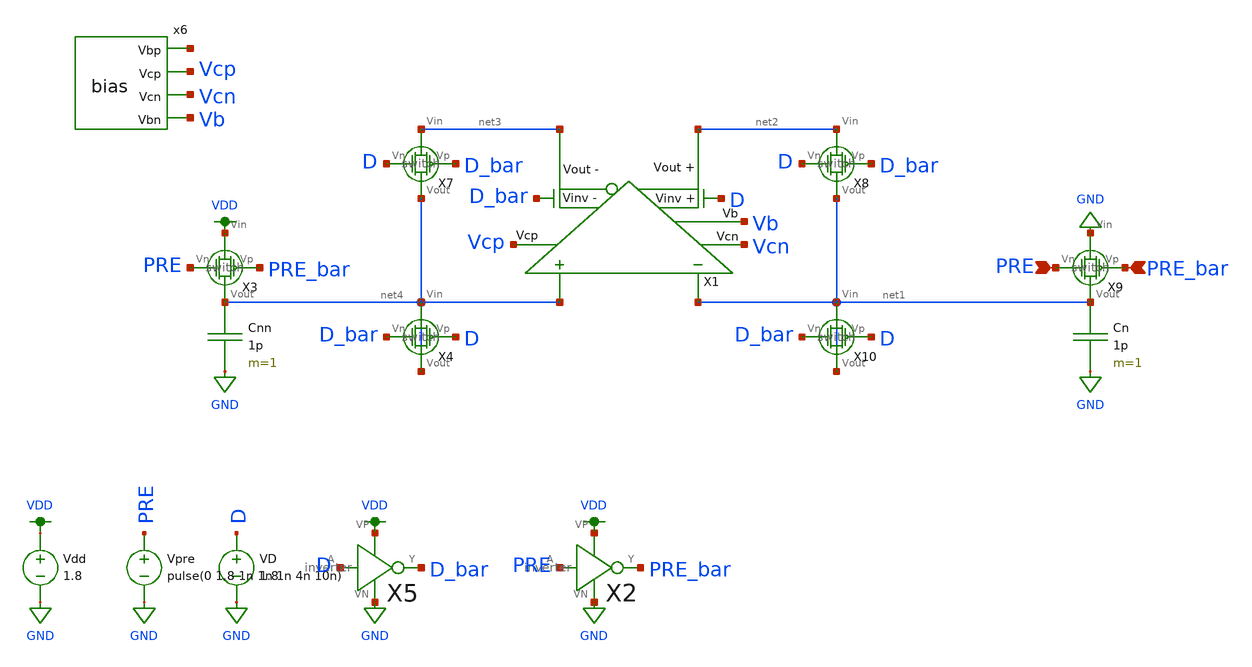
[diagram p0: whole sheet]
** sch_path: simulations/helpppp.sch
**.subckt helpppp PRE_bar PRE
*.ipin PRE_bar
*.ipin PRE
X1 D_bar net3 net2 Vcp Vb net1 net4 D Vcn ota W_U=12 L_U=0.5
Cn net1 GND 1p m=1
Cnn net4 GND 1p m=1
Vdd VDD GND 1.8
Vpre PRE GND pulse(0 1.8 1n 1n 1n 4n 10n)
X2 PRE PRE_bar VDD GND inverter
X5 D D_bar VDD GND inverter
VD D GND 1.8
x6 net5 Vcp Vcn Vb bias
X3 VDD net4 PRE_bar PRE switch W_U=12 L_U=0.5
X4 net4 net4 D D_bar switch W_U=12 L_U=0.5
X7 net3 net4 D_bar D switch W_U=12 L_U=0.5
X8 net2 net1 D_bar D switch W_U=12 L_U=0.5
X9 GND net1 PRE_bar PRE switch W_U=12 L_U=0.5
X10 net1 net1 D D_bar switch W_U=12 L_U=0.5
**** begin user architecture code

.option wnflag=1
.param MC_SWITCH=0.0
.lib ~/skywater/skywater-pdk/libraries/sky130_fd_pr_ngspice/latest/models/sky130.lib.spice tt


.tran 0.01n 200n
.save all

**** end user architecture code
**.ends

* expanding   symbol:  ../schematics/ota.sym # of pins=9
** sym_path: schematics/ota.sym
** sch_path: schematics/ota.sch
.subckt ota Vinv_n Vout_n Vout_p Vcp Vb Vin_n Vin_p Vinv_p Vcn  L_U=0.15 W_U=1
*.ipin Vin_n
*.ipin Vin_p
*.opin Vout_n
*.opin Vout_p
*.ipin Vcp
*.ipin Vb
*.ipin Vinv_p
*.ipin Vinv_n
*.ipin Vcn
XM18 net3 net3 VDD VDD sky130_fd_pr__pfet_01v8 L=L_U W=W_U nf=1 ad='int((nf+1)/2) * W/nf * 0.29' as='int((nf+2)/2) * W/nf * 0.29'
+ pd='2*int((nf+1)/2) * (W/nf + 0.29)' ps='2*int((nf+2)/2) * (W/nf + 0.29)' nrd='0.29 / W' nrs='0.29 / W'
+ sa=0 sb=0 sd=0 mult=1 m=1
XM19 net4 Vin_n net1 GND sky130_fd_pr__nfet_01v8 L=L_U W=W_U nf=1 ad='int((nf+1)/2) * W/nf * 0.29' as='int((nf+2)/2) * W/nf * 0.29'
+ pd='2*int((nf+1)/2) * (W/nf + 0.29)' ps='2*int((nf+2)/2) * (W/nf + 0.29)' nrd='0.29 / W' nrs='0.29 / W'
+ sa=0 sb=0 sd=0 mult=1 m=1
XM20 net3 Vin_p net1 GND sky130_fd_pr__nfet_01v8 L=L_U W=W_U nf=1 ad='int((nf+1)/2) * W/nf * 0.29' as='int((nf+2)/2) * W/nf * 0.29'
+ pd='2*int((nf+1)/2) * (W/nf + 0.29)' ps='2*int((nf+2)/2) * (W/nf + 0.29)' nrd='0.29 / W' nrs='0.29 / W'
+ sa=0 sb=0 sd=0 mult=1 m=1
XM21 net1 Vb GND GND sky130_fd_pr__nfet_01v8 L=L_U W=W_U nf=1 ad='int((nf+1)/2) * W/nf * 0.29' as='int((nf+2)/2) * W/nf * 0.29'
+ pd='2*int((nf+1)/2) * (W/nf + 0.29)' ps='2*int((nf+2)/2) * (W/nf + 0.29)' nrd='0.29 / W' nrs='0.29 / W'
+ sa=0 sb=0 sd=0 mult=1 m=1
XM22 net4 net4 VDD VDD sky130_fd_pr__pfet_01v8 L=L_U W=W_U nf=1 ad='int((nf+1)/2) * W/nf * 0.29' as='int((nf+2)/2) * W/nf * 0.29'
+ pd='2*int((nf+1)/2) * (W/nf + 0.29)' ps='2*int((nf+2)/2) * (W/nf + 0.29)' nrd='0.29 / W' nrs='0.29 / W'
+ sa=0 sb=0 sd=0 mult=1 m=1
XM23 net7 net3 VDD VDD sky130_fd_pr__pfet_01v8 L=L_U W=W_U nf=1 ad='int((nf+1)/2) * W/nf * 0.29' as='int((nf+2)/2) * W/nf * 0.29'
+ pd='2*int((nf+1)/2) * (W/nf + 0.29)' ps='2*int((nf+2)/2) * (W/nf + 0.29)' nrd='0.29 / W' nrs='0.29 / W'
+ sa=0 sb=0 sd=0 mult=1 m=1
XM24 net8 net4 VDD VDD sky130_fd_pr__pfet_01v8 L=L_U W=W_U nf=1 ad='int((nf+1)/2) * W/nf * 0.29' as='int((nf+2)/2) * W/nf * 0.29'
+ pd='2*int((nf+1)/2) * (W/nf + 0.29)' ps='2*int((nf+2)/2) * (W/nf + 0.29)' nrd='0.29 / W' nrs='0.29 / W'
+ sa=0 sb=0 sd=0 mult=1 m=1
XM25 net8 Vcp Vout_n VDD sky130_fd_pr__pfet_01v8 L=L_U W=W_U nf=1 ad='int((nf+1)/2) * W/nf * 0.29' as='int((nf+2)/2) * W/nf * 0.29'
+ pd='2*int((nf+1)/2) * (W/nf + 0.29)' ps='2*int((nf+2)/2) * (W/nf + 0.29)' nrd='0.29 / W' nrs='0.29 / W'
+ sa=0 sb=0 sd=0 mult=1 m=1
XM26 Vout_p Vcp net7 VDD sky130_fd_pr__pfet_01v8 L=L_U W=W_U nf=1 ad='int((nf+1)/2) * W/nf * 0.29' as='int((nf+2)/2) * W/nf * 0.29'
+ pd='2*int((nf+1)/2) * (W/nf + 0.29)' ps='2*int((nf+2)/2) * (W/nf + 0.29)' nrd='0.29 / W' nrs='0.29 / W'
+ sa=0 sb=0 sd=0 mult=1 m=1
XM27 Vout_p Vcn net6 GND sky130_fd_pr__nfet_01v8 L=L_U W=W_U nf=1 ad='int((nf+1)/2) * W/nf * 0.29' as='int((nf+2)/2) * W/nf * 0.29'
+ pd='2*int((nf+1)/2) * (W/nf + 0.29)' ps='2*int((nf+2)/2) * (W/nf + 0.29)' nrd='0.29 / W' nrs='0.29 / W'
+ sa=0 sb=0 sd=0 mult=1 m=1
XM28 Vout_n Vcn net2 GND sky130_fd_pr__nfet_01v8 L=L_U W=W_U nf=1 ad='int((nf+1)/2) * W/nf * 0.29' as='int((nf+2)/2) * W/nf * 0.29'
+ pd='2*int((nf+1)/2) * (W/nf + 0.29)' ps='2*int((nf+2)/2) * (W/nf + 0.29)' nrd='0.29 / W' nrs='0.29 / W'
+ sa=0 sb=0 sd=0 mult=1 m=1
XM29 net6 net5 GND GND sky130_fd_pr__nfet_01v8 L=L_U W=W_U nf=1 ad='int((nf+1)/2) * W/nf * 0.29' as='int((nf+2)/2) * W/nf * 0.29'
+ pd='2*int((nf+1)/2) * (W/nf + 0.29)' ps='2*int((nf+2)/2) * (W/nf + 0.29)' nrd='0.29 / W' nrs='0.29 / W'
+ sa=0 sb=0 sd=0 mult=1 m=1
XM30 Vout_p Vinv_p net5 GND sky130_fd_pr__nfet_01v8 L=L_U W=W_U nf=1 ad='int((nf+1)/2) * W/nf * 0.29'
+ as='int((nf+2)/2) * W/nf * 0.29' pd='2*int((nf+1)/2) * (W/nf + 0.29)' ps='2*int((nf+2)/2) * (W/nf + 0.29)'
+ nrd='0.29 / W' nrs='0.29 / W' sa=0 sb=0 sd=0 mult=1 m=1
XM32 net2 net5 GND GND sky130_fd_pr__nfet_01v8 L=L_U W=W_U nf=1 ad='int((nf+1)/2) * W/nf * 0.29' as='int((nf+2)/2) * W/nf * 0.29'
+ pd='2*int((nf+1)/2) * (W/nf + 0.29)' ps='2*int((nf+2)/2) * (W/nf + 0.29)' nrd='0.29 / W' nrs='0.29 / W'
+ sa=0 sb=0 sd=0 mult=1 m=1
XM34 Vout_n Vinv_n net5 GND sky130_fd_pr__nfet_01v8 L=L_U W=W_U nf=1 ad='int((nf+1)/2) * W/nf * 0.29'
+ as='int((nf+2)/2) * W/nf * 0.29' pd='2*int((nf+1)/2) * (W/nf + 0.29)' ps='2*int((nf+2)/2) * (W/nf + 0.29)'
+ nrd='0.29 / W' nrs='0.29 / W' sa=0 sb=0 sd=0 mult=1 m=1
.ends


* expanding   symbol:  ../schematics/inverter.sym # of pins=4
** sym_path: schematics/inverter.sym
** sch_path: schematics/inverter.sch
.subckt inverter A Y VP VN
*.ipin A
*.iopin VP
*.iopin VN
*.opin Y
XM1 Y A VP VDD sky130_fd_pr__pfet_01v8 L=0.15 W=1 nf=1 ad='int((nf+1)/2) * W/nf * 0.29' as='int((nf+2)/2) * W/nf * 0.29'
+ pd='2*int((nf+1)/2) * (W/nf + 0.29)' ps='2*int((nf+2)/2) * (W/nf + 0.29)' nrd='0.29 / W' nrs='0.29 / W'
+ sa=0 sb=0 sd=0 mult=1 m=1
XM2 Y A VN GND sky130_fd_pr__nfet_01v8 L=0.15 W=1 nf=1 ad='int((nf+1)/2) * W/nf * 0.29' as='int((nf+2)/2) * W/nf * 0.29'
+ pd='2*int((nf+1)/2) * (W/nf + 0.29)' ps='2*int((nf+2)/2) * (W/nf + 0.29)' nrd='0.29 / W' nrs='0.29 / W'
+ sa=0 sb=0 sd=0 mult=1 m=1
.ends


* expanding   symbol:  ../schematics/bias.sym # of pins=4
** sym_path: schematics/bias.sym
** sch_path: schematics/bias.sch
.subckt bias Vbp Vcp Vcn Vbn
*.opin Vcp
*.opin Vcn
*.opin Vbn
*.opin Vbp
XM1 net1 Vbn GND GND sky130_fd_pr__nfet_01v8 L=2.5 W=12 nf=1 ad='int((nf+1)/2) * W/nf * 0.29' as='int((nf+2)/2) * W/nf * 0.29'
+ pd='2*int((nf+1)/2) * (W/nf + 0.29)' ps='2*int((nf+2)/2) * (W/nf + 0.29)' nrd='0.29 / W' nrs='0.29 / W'
+ sa=0 sb=0 sd=0 mult=1 m=1
XM2 Vcp Vbn GND GND sky130_fd_pr__nfet_01v8 L=0.5 W=12 nf=1 ad='int((nf+1)/2) * W/nf * 0.29' as='int((nf+2)/2) * W/nf * 0.29'
+ pd='2*int((nf+1)/2) * (W/nf + 0.29)' ps='2*int((nf+2)/2) * (W/nf + 0.29)' nrd='0.29 / W' nrs='0.29 / W'
+ sa=0 sb=0 sd=0 mult=1 m=1
XM3 Vbp Vbn GND GND sky130_fd_pr__nfet_01v8 L=0.5 W=12 nf=1 ad='int((nf+1)/2) * W/nf * 0.29' as='int((nf+2)/2) * W/nf * 0.29'
+ pd='2*int((nf+1)/2) * (W/nf + 0.29)' ps='2*int((nf+2)/2) * (W/nf + 0.29)' nrd='0.29 / W' nrs='0.29 / W'
+ sa=0 sb=0 sd=0 mult=1 m=1
XM4 net3 net4 GND GND sky130_fd_pr__nfet_01v8 L=0.5 W=12 nf=1 ad='int((nf+1)/2) * W/nf * 0.29' as='int((nf+2)/2) * W/nf * 0.29'
+ pd='2*int((nf+1)/2) * (W/nf + 0.29)' ps='2*int((nf+2)/2) * (W/nf + 0.29)' nrd='0.29 / W' nrs='0.29 / W'
+ sa=0 sb=0 sd=0 mult=1 m=1
XM5 Vbn Vbn GND GND sky130_fd_pr__nfet_01v8 L=0.5 W=12 nf=1 ad='int((nf+1)/2) * W/nf * 0.29' as='int((nf+2)/2) * W/nf * 0.29'
+ pd='2*int((nf+1)/2) * (W/nf + 0.29)' ps='2*int((nf+2)/2) * (W/nf + 0.29)' nrd='0.29 / W' nrs='0.29 / W'
+ sa=0 sb=0 sd=0 mult=1 m=1
XM6 net4 net4 net3 GND sky130_fd_pr__nfet_01v8 L=0.5 W=48 nf=1 ad='int((nf+1)/2) * W/nf * 0.29' as='int((nf+2)/2) * W/nf * 0.29'
+ pd='2*int((nf+1)/2) * (W/nf + 0.29)' ps='2*int((nf+2)/2) * (W/nf + 0.29)' nrd='0.29 / W' nrs='0.29 / W'
+ sa=0 sb=0 sd=0 mult=1 m=1
XM7 Vcn Vcn net3 GND sky130_fd_pr__nfet_01v8 L=0.5 W=12 nf=1 ad='int((nf+1)/2) * W/nf * 0.29' as='int((nf+2)/2) * W/nf * 0.29'
+ pd='2*int((nf+1)/2) * (W/nf + 0.29)' ps='2*int((nf+2)/2) * (W/nf + 0.29)' nrd='0.29 / W' nrs='0.29 / W'
+ sa=0 sb=0 sd=0 mult=1 m=1
XM8 net1 net1 net2 VDD sky130_fd_pr__pfet_01v8 L=0.5 W=48 nf=1 ad='int((nf+1)/2) * W/nf * 0.29' as='int((nf+2)/2) * W/nf * 0.29'
+ pd='2*int((nf+1)/2) * (W/nf + 0.29)' ps='2*int((nf+2)/2) * (W/nf + 0.29)' nrd='0.29 / W' nrs='0.29 / W'
+ sa=0 sb=0 sd=0 mult=1 m=1
XM9 net2 net1 VDD VDD sky130_fd_pr__pfet_01v8 L=0.5 W=12 nf=1 ad='int((nf+1)/2) * W/nf * 0.29' as='int((nf+2)/2) * W/nf * 0.29'
+ pd='2*int((nf+1)/2) * (W/nf + 0.29)' ps='2*int((nf+2)/2) * (W/nf + 0.29)' nrd='0.29 / W' nrs='0.29 / W'
+ sa=0 sb=0 sd=0 mult=1 m=1
XM10 Vcp Vcp net2 VDD sky130_fd_pr__pfet_01v8 L=0.5 W=12 nf=1 ad='int((nf+1)/2) * W/nf * 0.29' as='int((nf+2)/2) * W/nf * 0.29'
+ pd='2*int((nf+1)/2) * (W/nf + 0.29)' ps='2*int((nf+2)/2) * (W/nf + 0.29)' nrd='0.29 / W' nrs='0.29 / W'
+ sa=0 sb=0 sd=0 mult=1 m=1
XM11 Vbp Vbp VDD VDD sky130_fd_pr__pfet_01v8 L=0.5 W=12 nf=1 ad='int((nf+1)/2) * W/nf * 0.29' as='int((nf+2)/2) * W/nf * 0.29'
+ pd='2*int((nf+1)/2) * (W/nf + 0.29)' ps='2*int((nf+2)/2) * (W/nf + 0.29)' nrd='0.29 / W' nrs='0.29 / W'
+ sa=0 sb=0 sd=0 mult=1 m=1
XM12 net4 Vbp VDD VDD sky130_fd_pr__pfet_01v8 L=2.5 W=12 nf=1 ad='int((nf+1)/2) * W/nf * 0.29' as='int((nf+2)/2) * W/nf * 0.29'
+ pd='2*int((nf+1)/2) * (W/nf + 0.29)' ps='2*int((nf+2)/2) * (W/nf + 0.29)' nrd='0.29 / W' nrs='0.29 / W'
+ sa=0 sb=0 sd=0 mult=1 m=1
XM13 Vcn Vbp VDD VDD sky130_fd_pr__pfet_01v8 L=0.5 W=12 nf=1 ad='int((nf+1)/2) * W/nf * 0.29' as='int((nf+2)/2) * W/nf * 0.29'
+ pd='2*int((nf+1)/2) * (W/nf + 0.29)' ps='2*int((nf+2)/2) * (W/nf + 0.29)' nrd='0.29 / W' nrs='0.29 / W'
+ sa=0 sb=0 sd=0 mult=1 m=1
I1 VDD Vbn 100u
.ends


* expanding   symbol:  /home/madvlsi/algorithmic-ada-converter/schematics/switch.sym # of pins=4
** sym_path: schematics/switch.sym
** sch_path: schematics/switch.sch
.subckt switch Vin Vout Vp Vn  W_U=12 L_U=0.5
*.iopin Vin
*.iopin Vout
*.ipin Vp
*.ipin Vn
XM24 Vin Vp Vout VDD sky130_fd_pr__pfet_01v8 L=L_U W=W_U nf=1 ad='int((nf+1)/2) * W/nf * 0.29' as='int((nf+2)/2) * W/nf * 0.29'
+ pd='2*int((nf+1)/2) * (W/nf + 0.29)' ps='2*int((nf+2)/2) * (W/nf + 0.29)' nrd='0.29 / W' nrs='0.29 / W'
+ sa=0 sb=0 sd=0 mult=2 m=2
XM25 Vout Vn Vin GND sky130_fd_pr__nfet_01v8 L=L_U W=W_U nf=1 ad='int((nf+1)/2) * W/nf * 0.29' as='int((nf+2)/2) * W/nf * 0.29'
+ pd='2*int((nf+1)/2) * (W/nf + 0.29)' ps='2*int((nf+2)/2) * (W/nf + 0.29)' nrd='0.29 / W' nrs='0.29 / W'
+ sa=0 sb=0 sd=0 mult=1 m=1
.ends

.GLOBAL GND
.GLOBAL VDD
.end
